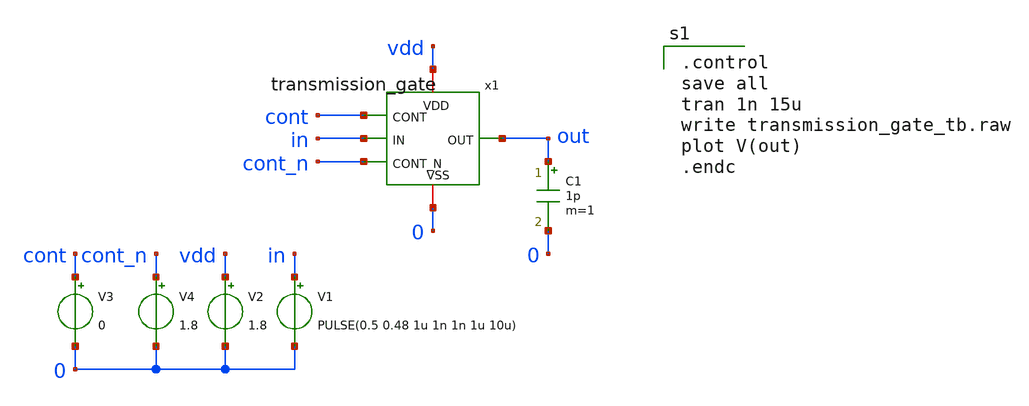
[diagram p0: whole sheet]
** sch_path: xschem/transmission_gate_tb.sch
**.subckt transmission_gate_tb
V1 in 0 PULSE(0.5 0.48 1u 1n 1n 1u 10u)
V2 vdd 0 1.8
V3 cont 0 0
C1 out 0 1p m=1
x1 vdd out in cont 0 cont_n transmission_gate W=20 L=1 NF=1 M=1
V4 cont_n 0 1.8
**** begin user architecture code

.control
save all
tran 1n 15u
write transmission_gate_tb.raw
plot V(out)
.endc


** opencircuitdesign pdks install
.lib $::SKYWATER_MODELS/sky130.lib.spice tt


**** end user architecture code
**.ends

* expanding   symbol:  /foss/designs/Transmission-Gate/xschem/transmission_gate.sym # of pins=6
** sym_path: xschem/transmission_gate.sym
** sch_path: xschem/transmission_gate.sch
.subckt transmission_gate VDD OUT IN CONT VSS CONT_N  W=20 L=1 NF=1 M=1
*.opin OUT
*.ipin IN
*.iopin VDD
*.iopin VSS
*.ipin CONT
*.ipin CONT_N
XM2 IN CONT OUT VSS sky130_fd_pr__nfet_01v8 L=L W=W nf=NF ad='int((NF + 1)/2) * W / NF * 0.29' as='int((NF + 2)/2) * W / NF * 0.29'
+ pd='2*int((NF + 1)/2) * (W / NF + 0.29)' ps='2*int((NF + 2)/2) * (W / NF + 0.29)' nrd='0.29 / W ' nrs='0.29 / W '
+ sa=0 sb=0 sd=0 mult=M m=M
XM11 IN CONT_N OUT VDD sky130_fd_pr__pfet_01v8 L=L W=W nf=NF ad='int((nf+1)/2) * W/nf * 0.29' as='int((nf+2)/2) * W/nf * 0.29'
+ pd='2*int((nf+1)/2) * (W/nf + 0.29)' ps='2*int((nf+2)/2) * (W/nf + 0.29)' nrd='0.29 / W' nrs='0.29 / W'
+ sa=0 sb=0 sd=0 mult=M m=M
.ends

.end
